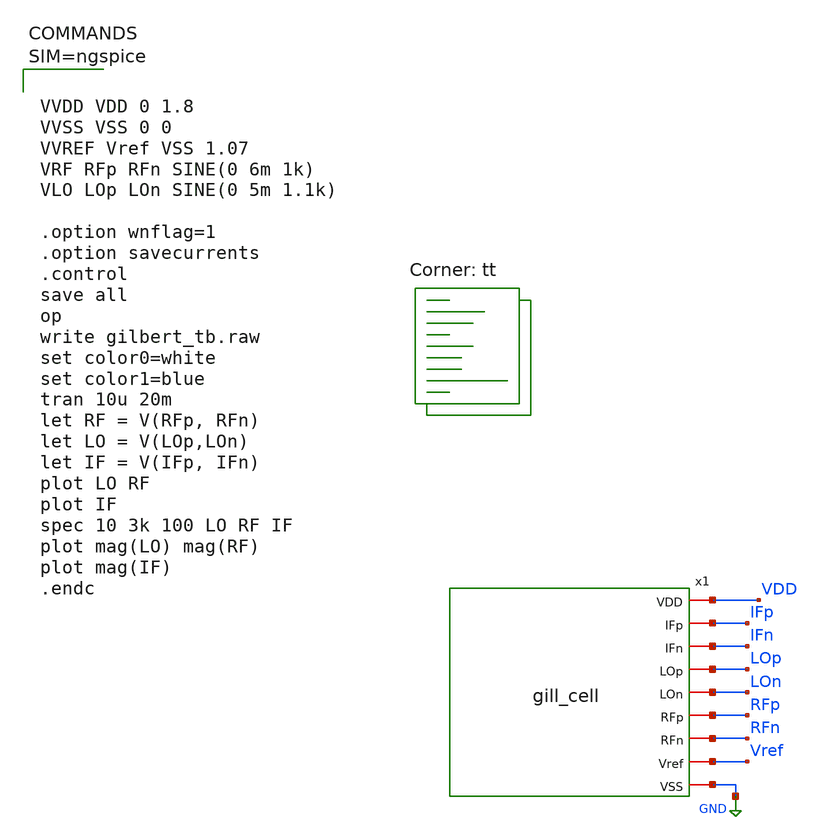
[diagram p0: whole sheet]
** sch_path: hw07/xschem/gilbert_tb.sch
**.subckt gilbert_tb
x1 VDD IFp IFn LOp LOn RFp RFn Vref GND gill_cell
**** begin user architecture code



VVDD VDD 0 1.8
VVSS VSS 0 0
VVREF Vref VSS 1.07
VRF RFp RFn SINE(0 6m 1k)
VLO LOp LOn SINE(0 5m 1.1k)

.option wnflag=1
.option savecurrents
.control
save all
op
write gilbert_tb.raw
set color0=white
set color1=blue
tran 10u 20m
let RF = V(RFp, RFn)
let LO = V(LOp,LOn)
let IF = V(IFp, IFn)
plot LO RF
plot IF
spec 10 3k 100 LO RF IF
plot mag(LO) mag(RF)
plot mag(IF)
.endc



.lib $::SKYWATER_MODELS/sky130.lib.spice tt
**** end user architecture code
**.ends

* expanding   symbol:  gill_cell.sym # of pins=9
** sym_path: hw07/xschem/gill_cell.sym
** sch_path: hw07/xschem/gill_cell.sch
.subckt gill_cell VDD IFp IFn LOp LOn RFp RFn Vref VSS
*.iopin IFp
*.iopin IFn
*.iopin LOp
*.iopin LOn
*.iopin RFp
*.iopin RFn
*.iopin VDD
*.iopin VSS
*.iopin Vref
XR1 IF++ VDD VSS sky130_fd_pr__res_xhigh_po_0p69 L=6.9 mult=1 m=1
XR3 IF-- VDD VSS sky130_fd_pr__res_xhigh_po_0p69 L=6.9 mult=1 m=1
XR10 VDD LOp VSS sky130_fd_pr__res_xhigh_po_0p69 L=1.38 mult=1 m=1
XR11 LOp VSS VSS sky130_fd_pr__res_xhigh_po_0p69 L=3.45 mult=1 m=1
XR6 VDD RFn VSS sky130_fd_pr__res_xhigh_po_0p69 L=0.69*7 mult=1 m=1
XR7 RFn VSS VSS sky130_fd_pr__res_xhigh_po_0p69 L=3.45 mult=1 m=1
XR8 VDD RFp VSS sky130_fd_pr__res_xhigh_po_0p69 L=0.69*7 mult=1 m=1
XR9 RFp VSS VSS sky130_fd_pr__res_xhigh_po_0p69 L=3.45 mult=1 m=1
XR12 LOn VDD VSS sky130_fd_pr__res_xhigh_po_0p69 L=1.38 mult=1 m=1
XR13 VSS LOn VSS sky130_fd_pr__res_xhigh_po_0p69 L=3.45 mult=1 m=1
XM2 net1 VM VSS VSS sky130_fd_pr__nfet_01v8 L=1.1 W=40 nf=1 ad='int((nf+1)/2) * W/nf * 0.29' as='int((nf+2)/2) * W/nf * 0.29'
+ pd='2*int((nf+1)/2) * (W/nf + 0.29)' ps='2*int((nf+2)/2) * (W/nf + 0.29)' nrd='0.29 / W' nrs='0.29 / W'
+ sa=0 sb=0 sd=0 mult=1 m=1
XM3 Vmid RFp net1 VSS sky130_fd_pr__nfet_01v8 L=1.1 W=40 nf=1 ad='int((nf+1)/2) * W/nf * 0.29' as='int((nf+2)/2) * W/nf * 0.29'
+ pd='2*int((nf+1)/2) * (W/nf + 0.29)' ps='2*int((nf+2)/2) * (W/nf + 0.29)' nrd='0.29 / W' nrs='0.29 / W'
+ sa=0 sb=0 sd=0 mult=1 m=1
XM5 IF++ LOp Vmid VSS sky130_fd_pr__nfet_01v8 L=1.1 W=40 nf=1 ad='int((nf+1)/2) * W/nf * 0.29' as='int((nf+2)/2) * W/nf * 0.29'
+ pd='2*int((nf+1)/2) * (W/nf + 0.29)' ps='2*int((nf+2)/2) * (W/nf + 0.29)' nrd='0.29 / W' nrs='0.29 / W'
+ sa=0 sb=0 sd=0 mult=1 m=1
XM7 IF++ LOn Vmid2 VSS sky130_fd_pr__nfet_01v8 L=1.1 W=40 nf=1 ad='int((nf+1)/2) * W/nf * 0.29' as='int((nf+2)/2) * W/nf * 0.29'
+ pd='2*int((nf+1)/2) * (W/nf + 0.29)' ps='2*int((nf+2)/2) * (W/nf + 0.29)' nrd='0.29 / W' nrs='0.29 / W'
+ sa=0 sb=0 sd=0 mult=1 m=1
XM4 Vmid2 RFn net1 VSS sky130_fd_pr__nfet_01v8 L=1.1 W=40 nf=1 ad='int((nf+1)/2) * W/nf * 0.29' as='int((nf+2)/2) * W/nf * 0.29'
+ pd='2*int((nf+1)/2) * (W/nf + 0.29)' ps='2*int((nf+2)/2) * (W/nf + 0.29)' nrd='0.29 / W' nrs='0.29 / W'
+ sa=0 sb=0 sd=0 mult=1 m=1
XM8 IF-- LOp Vmid2 VSS sky130_fd_pr__nfet_01v8 L=1.1 W=40 nf=1 ad='int((nf+1)/2) * W/nf * 0.29' as='int((nf+2)/2) * W/nf * 0.29'
+ pd='2*int((nf+1)/2) * (W/nf + 0.29)' ps='2*int((nf+2)/2) * (W/nf + 0.29)' nrd='0.29 / W' nrs='0.29 / W'
+ sa=0 sb=0 sd=0 mult=1 m=1
XM6 IF-- LOn Vmid VSS sky130_fd_pr__nfet_01v8 L=1.1 W=40 nf=1 ad='int((nf+1)/2) * W/nf * 0.29' as='int((nf+2)/2) * W/nf * 0.29'
+ pd='2*int((nf+1)/2) * (W/nf + 0.29)' ps='2*int((nf+2)/2) * (W/nf + 0.29)' nrd='0.29 / W' nrs='0.29 / W'
+ sa=0 sb=0 sd=0 mult=1 m=1
XM9 Vamp VM VSS VSS sky130_fd_pr__nfet_01v8 L=1.1 W=40 nf=1 ad='int((nf+1)/2) * W/nf * 0.29' as='int((nf+2)/2) * W/nf * 0.29'
+ pd='2*int((nf+1)/2) * (W/nf + 0.29)' ps='2*int((nf+2)/2) * (W/nf + 0.29)' nrd='0.29 / W' nrs='0.29 / W'
+ sa=0 sb=0 sd=0 mult=1 m=1
XM10 IFn IF++ Vamp VSS sky130_fd_pr__nfet_01v8 L=1.1 W=40 nf=1 ad='int((nf+1)/2) * W/nf * 0.29' as='int((nf+2)/2) * W/nf * 0.29'
+ pd='2*int((nf+1)/2) * (W/nf + 0.29)' ps='2*int((nf+2)/2) * (W/nf + 0.29)' nrd='0.29 / W' nrs='0.29 / W'
+ sa=0 sb=0 sd=0 mult=1 m=1
XM11 IFp IF-- Vamp VSS sky130_fd_pr__nfet_01v8 L=1.1 W=40 nf=1 ad='int((nf+1)/2) * W/nf * 0.29' as='int((nf+2)/2) * W/nf * 0.29'
+ pd='2*int((nf+1)/2) * (W/nf + 0.29)' ps='2*int((nf+2)/2) * (W/nf + 0.29)' nrd='0.29 / W' nrs='0.29 / W'
+ sa=0 sb=0 sd=0 mult=1 m=1
XR14 IFp VDD VSS sky130_fd_pr__res_xhigh_po_0p69 L=9.67 mult=1 m=1
XR15 IFn VDD VSS sky130_fd_pr__res_xhigh_po_0p69 L=9.67 mult=1 m=1
XM1 net2 Vref VSS VSS sky130_fd_pr__nfet_01v8 L=4 W=1 nf=1 ad='int((nf+1)/2) * W/nf * 0.29' as='int((nf+2)/2) * W/nf * 0.29'
+ pd='2*int((nf+1)/2) * (W/nf + 0.29)' ps='2*int((nf+2)/2) * (W/nf + 0.29)' nrd='0.29 / W' nrs='0.29 / W'
+ sa=0 sb=0 sd=0 mult=1 m=1
XM12 VM VM VSS VSS sky130_fd_pr__nfet_01v8 L=2 W=1 nf=1 ad='int((nf+1)/2) * W/nf * 0.29' as='int((nf+2)/2) * W/nf * 0.29'
+ pd='2*int((nf+1)/2) * (W/nf + 0.29)' ps='2*int((nf+2)/2) * (W/nf + 0.29)' nrd='0.29 / W' nrs='0.29 / W'
+ sa=0 sb=0 sd=0 mult=1 m=1
XM15 VM net2 VDD VDD sky130_fd_pr__pfet_01v8 L=16 W=1 nf=1 ad='int((nf+1)/2) * W/nf * 0.29' as='int((nf+2)/2) * W/nf * 0.29'
+ pd='2*int((nf+1)/2) * (W/nf + 0.29)' ps='2*int((nf+2)/2) * (W/nf + 0.29)' nrd='0.29 / W' nrs='0.29 / W'
+ sa=0 sb=0 sd=0 mult=1 m=1
XM13 net2 net2 VDD VDD sky130_fd_pr__pfet_01v8 L=16 W=1 nf=1 ad='int((nf+1)/2) * W/nf * 0.29' as='int((nf+2)/2) * W/nf * 0.29'
+ pd='2*int((nf+1)/2) * (W/nf + 0.29)' ps='2*int((nf+2)/2) * (W/nf + 0.29)' nrd='0.29 / W' nrs='0.29 / W'
+ sa=0 sb=0 sd=0 mult=1 m=1
.ends

.GLOBAL GND
.end
